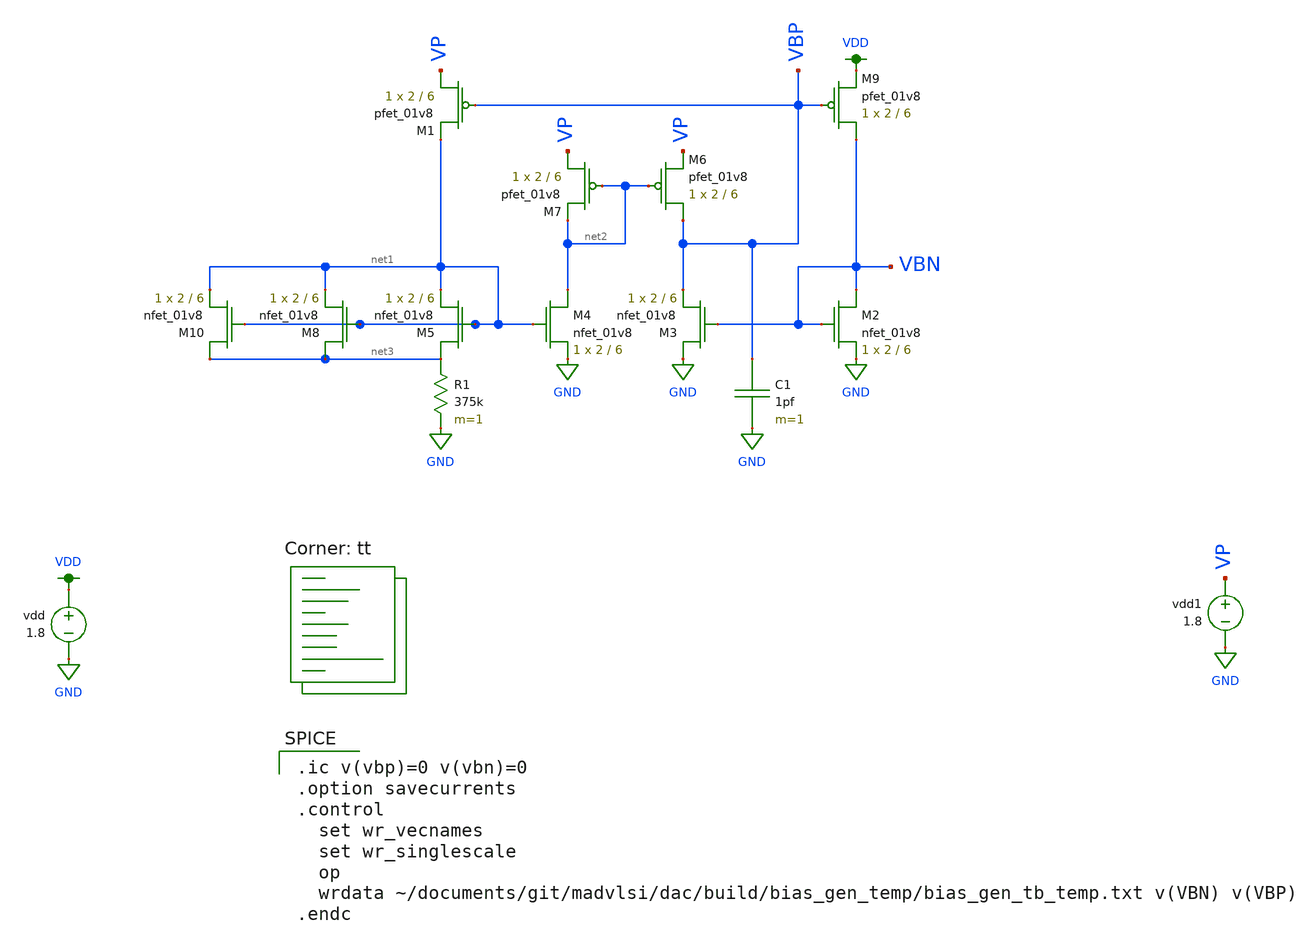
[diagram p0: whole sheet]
** sch_path: dac/schematic/bias_gen_tb_temp.sch
**.subckt bias_gen_tb_temp
vdd VDD GND 1.8
R1 net3 GND 375k m=1
XM5 net3 net1 net1 GND sky130_fd_pr__nfet_01v8 L=6 W=2 nf=1 ad='int((nf+1)/2) * W/nf * 0.29' as='int((nf+2)/2) * W/nf * 0.29'
+ pd='2*int((nf+1)/2) * (W/nf + 0.29)' ps='2*int((nf+2)/2) * (W/nf + 0.29)' nrd='0.29 / W' nrs='0.29 / W'
+ sa=0 sb=0 sd=0 mult=1 m=1
XM2 VBN VBN GND GND sky130_fd_pr__nfet_01v8 L=6 W=2 nf=1 ad='int((nf+1)/2) * W/nf * 0.29' as='int((nf+2)/2) * W/nf * 0.29'
+ pd='2*int((nf+1)/2) * (W/nf + 0.29)' ps='2*int((nf+2)/2) * (W/nf + 0.29)' nrd='0.29 / W' nrs='0.29 / W'
+ sa=0 sb=0 sd=0 mult=1 m=1
XM9 VBN VBP VDD VDD sky130_fd_pr__pfet_01v8 L=6 W=2 nf=1 ad='int((nf+1)/2) * W/nf * 0.29' as='int((nf+2)/2) * W/nf * 0.29'
+ pd='2*int((nf+1)/2) * (W/nf + 0.29)' ps='2*int((nf+2)/2) * (W/nf + 0.29)' nrd='0.29 / W' nrs='0.29 / W'
+ sa=0 sb=0 sd=0 mult=1 m=1
XM1 VP VBP net1 VDD sky130_fd_pr__pfet_01v8 L=6 W=2 nf=1 ad='int((nf+1)/2) * W/nf * 0.29' as='int((nf+2)/2) * W/nf * 0.29'
+ pd='2*int((nf+1)/2) * (W/nf + 0.29)' ps='2*int((nf+2)/2) * (W/nf + 0.29)' nrd='0.29 / W' nrs='0.29 / W'
+ sa=0 sb=0 sd=0 mult=1 m=1
XM3 GND VBN VBP GND sky130_fd_pr__nfet_01v8 L=6 W=2 nf=1 ad='int((nf+1)/2) * W/nf * 0.29' as='int((nf+2)/2) * W/nf * 0.29'
+ pd='2*int((nf+1)/2) * (W/nf + 0.29)' ps='2*int((nf+2)/2) * (W/nf + 0.29)' nrd='0.29 / W' nrs='0.29 / W'
+ sa=0 sb=0 sd=0 mult=1 m=1
XM4 net2 net1 GND GND sky130_fd_pr__nfet_01v8 L=6 W=2 nf=1 ad='int((nf+1)/2) * W/nf * 0.29' as='int((nf+2)/2) * W/nf * 0.29'
+ pd='2*int((nf+1)/2) * (W/nf + 0.29)' ps='2*int((nf+2)/2) * (W/nf + 0.29)' nrd='0.29 / W' nrs='0.29 / W'
+ sa=0 sb=0 sd=0 mult=1 m=1
XM6 VBP net2 VP VDD sky130_fd_pr__pfet_01v8 L=6 W=2 nf=1 ad='int((nf+1)/2) * W/nf * 0.29' as='int((nf+2)/2) * W/nf * 0.29'
+ pd='2*int((nf+1)/2) * (W/nf + 0.29)' ps='2*int((nf+2)/2) * (W/nf + 0.29)' nrd='0.29 / W' nrs='0.29 / W'
+ sa=0 sb=0 sd=0 mult=1 m=1
XM7 VP net2 net2 VDD sky130_fd_pr__pfet_01v8 L=6 W=2 nf=1 ad='int((nf+1)/2) * W/nf * 0.29' as='int((nf+2)/2) * W/nf * 0.29'
+ pd='2*int((nf+1)/2) * (W/nf + 0.29)' ps='2*int((nf+2)/2) * (W/nf + 0.29)' nrd='0.29 / W' nrs='0.29 / W'
+ sa=0 sb=0 sd=0 mult=1 m=1
C1 VBP GND 1pf m=1
XM8 net3 net1 net1 GND sky130_fd_pr__nfet_01v8 L=6 W=2 nf=1 ad='int((nf+1)/2) * W/nf * 0.29' as='int((nf+2)/2) * W/nf * 0.29'
+ pd='2*int((nf+1)/2) * (W/nf + 0.29)' ps='2*int((nf+2)/2) * (W/nf + 0.29)' nrd='0.29 / W' nrs='0.29 / W'
+ sa=0 sb=0 sd=0 mult=1 m=1
XM10 net3 net1 net1 GND sky130_fd_pr__nfet_01v8 L=6 W=2 nf=1 ad='int((nf+1)/2) * W/nf * 0.29' as='int((nf+2)/2) * W/nf * 0.29'
+ pd='2*int((nf+1)/2) * (W/nf + 0.29)' ps='2*int((nf+2)/2) * (W/nf + 0.29)' nrd='0.29 / W' nrs='0.29 / W'
+ sa=0 sb=0 sd=0 mult=1 m=1
vdd1 VP GND 1.8
**** begin user architecture code
.lib $::SKYWATER_MODELS/sky130.lib.spice tt

.ic v(vbp)=0 v(vbn)=0
.option savecurrents
.control
  set wr_vecnames
  set wr_singlescale
  op
  wrdata ~/documents/git/madvlsi/dac/build/bias_gen_temp/bias_gen_tb_temp.txt v(VBN) v(VBP)
.endc

**** end user architecture code
**.ends
.GLOBAL GND
.GLOBAL VDD
.end
